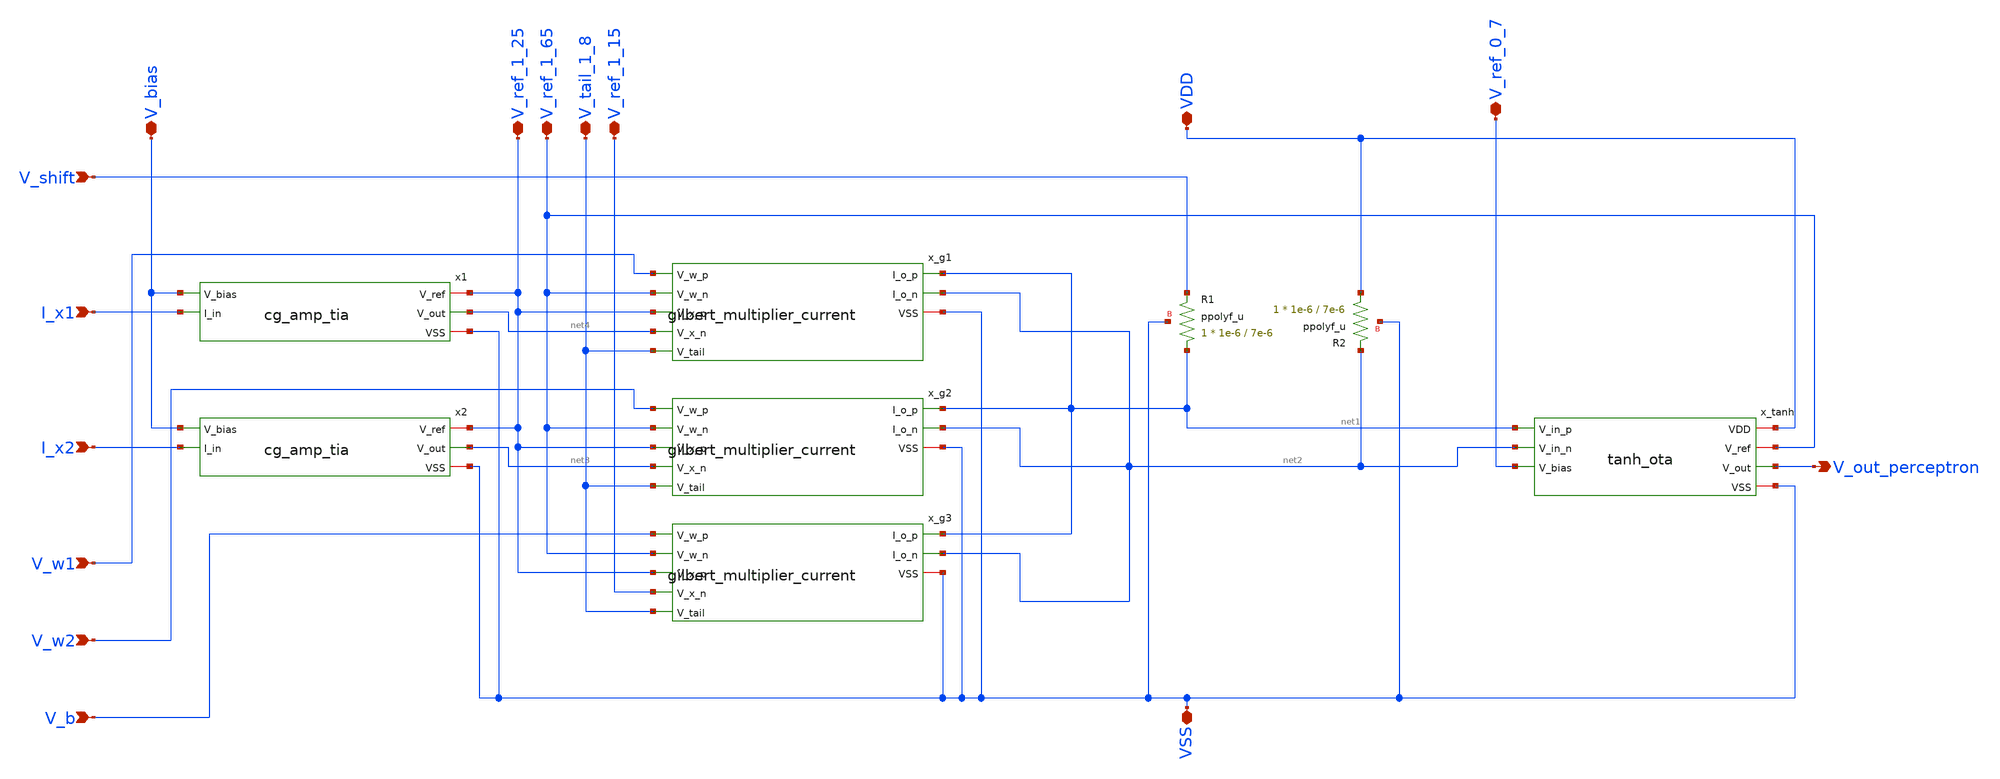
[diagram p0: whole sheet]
** sch_path: schematics/perceptron.sch
**.subckt perceptron VDD VSS V_bias I_x1 I_x2 V_ref_1_25 V_ref_1_15 V_ref_1_65 V_tail_1_8 V_w1 V_w2
*+ V_b V_ref_0_7 V_out_perceptron V_shift
*.iopin VDD
*.iopin VSS
*.iopin V_bias
*.ipin I_x1
*.ipin I_x2
*.iopin V_ref_1_25
*.iopin V_ref_1_15
*.iopin V_ref_1_65
*.iopin V_tail_1_8
*.ipin V_w1
*.ipin V_w2
*.ipin V_b
*.iopin V_ref_0_7
*.opin V_out_perceptron
*.ipin V_shift
x1 V_ref_1_25 net4 V_bias I_x1 VSS cg_amp_tia
x2 V_ref_1_25 net3 V_bias I_x2 VSS cg_amp_tia
x_g1 net1 net2 V_w1 V_ref_1_65 V_ref_1_25 net4 V_tail_1_8 VSS gilbert_multiplier_current
x_g2 net1 net2 V_w2 V_ref_1_65 V_ref_1_25 net3 V_tail_1_8 VSS gilbert_multiplier_current
x_g3 net1 net2 V_b V_ref_1_65 V_ref_1_25 V_ref_1_15 V_tail_1_8 VSS gilbert_multiplier_current
x_tanh VDD V_ref_1_65 V_out_perceptron net1 net2 V_ref_0_7 VSS tanh_ota
XR1 net1 V_shift VSS ppolyf_u r_width=1e-6 r_length=7e-6 m=1
XR2 VDD net2 VSS ppolyf_u r_width=1e-6 r_length=7e-6 m=1
**.ends

* expanding   symbol:  analog-perceptron-gf180mcu/schematics/cg_amp_tia.sym # of pins=5
** sym_path: schematics/cg_amp_tia.sym
** sch_path: schematics/cg_amp_tia.sch
.subckt cg_amp_tia V_ref V_out V_bias I_in VSS
*.iopin V_ref
*.iopin VSS
*.ipin I_in
*.ipin V_bias
*.opin V_out
XM1 V_out V_bias I_in VSS nfet_03v3 L=0.5u W=5u nf=1 ad='int((nf+1)/2) * W/nf * 0.18u' as='int((nf+2)/2) * W/nf * 0.18u'
+ pd='2*int((nf+1)/2) * (W/nf + 0.18u)' ps='2*int((nf+2)/2) * (W/nf + 0.18u)' nrd='0.18u / W' nrs='0.18u / W'
+ sa=0 sb=0 sd=0 m=1
XR1 V_out V_ref VSS ppolyf_u_1k r_width=3e-6 r_length=8.1e-6 m=1
.ends


* expanding   symbol:  analog-perceptron-gf180mcu/schematics/gilbert_multiplier_current.sym # of
*+ pins=8
** sym_path: schematics/gilbert_multiplier_current.sym
** sch_path: schematics/gilbert_multiplier_current.sch
.subckt gilbert_multiplier_current I_o_p I_o_n V_w_p V_w_n V_x_p V_x_n V_tail VSS
*.ipin V_x_p
*.ipin V_x_n
*.ipin V_tail
*.iopin VSS
*.ipin V_w_p
*.ipin V_w_n
*.opin I_o_n
*.opin I_o_p
XM1 net1 V_x_p net3 VSS nfet_03v3 L=0.5u W=10u nf=1 ad='int((nf+1)/2) * W/nf * 0.18u' as='int((nf+2)/2) * W/nf * 0.18u'
+ pd='2*int((nf+1)/2) * (W/nf + 0.18u)' ps='2*int((nf+2)/2) * (W/nf + 0.18u)' nrd='0.18u / W' nrs='0.18u / W'
+ sa=0 sb=0 sd=0 m=1
XM2 net2 V_x_n net4 VSS nfet_03v3 L=0.5u W=10u nf=1 ad='int((nf+1)/2) * W/nf * 0.18u' as='int((nf+2)/2) * W/nf * 0.18u'
+ pd='2*int((nf+1)/2) * (W/nf + 0.18u)' ps='2*int((nf+2)/2) * (W/nf + 0.18u)' nrd='0.18u / W' nrs='0.18u / W'
+ sa=0 sb=0 sd=0 m=1
XM3 I_o_n V_w_p net1 VSS nfet_03v3 L=0.5u W=10u nf=1 ad='int((nf+1)/2) * W/nf * 0.18u' as='int((nf+2)/2) * W/nf * 0.18u'
+ pd='2*int((nf+1)/2) * (W/nf + 0.18u)' ps='2*int((nf+2)/2) * (W/nf + 0.18u)' nrd='0.18u / W' nrs='0.18u / W'
+ sa=0 sb=0 sd=0 m=1
XM4 I_o_p V_w_n net1 VSS nfet_03v3 L=0.5u W=10u nf=1 ad='int((nf+1)/2) * W/nf * 0.18u' as='int((nf+2)/2) * W/nf * 0.18u'
+ pd='2*int((nf+1)/2) * (W/nf + 0.18u)' ps='2*int((nf+2)/2) * (W/nf + 0.18u)' nrd='0.18u / W' nrs='0.18u / W'
+ sa=0 sb=0 sd=0 m=1
XM5 I_o_n V_w_n net2 VSS nfet_03v3 L=0.5u W=10u nf=1 ad='int((nf+1)/2) * W/nf * 0.18u' as='int((nf+2)/2) * W/nf * 0.18u'
+ pd='2*int((nf+1)/2) * (W/nf + 0.18u)' ps='2*int((nf+2)/2) * (W/nf + 0.18u)' nrd='0.18u / W' nrs='0.18u / W'
+ sa=0 sb=0 sd=0 m=1
XM6 I_o_p V_w_p net2 VSS nfet_03v3 L=0.5u W=10u nf=1 ad='int((nf+1)/2) * W/nf * 0.18u' as='int((nf+2)/2) * W/nf * 0.18u'
+ pd='2*int((nf+1)/2) * (W/nf + 0.18u)' ps='2*int((nf+2)/2) * (W/nf + 0.18u)' nrd='0.18u / W' nrs='0.18u / W'
+ sa=0 sb=0 sd=0 m=1
XM7 net3 V_tail VSS VSS nfet_03v3 L=1u W=5u nf=1 ad='int((nf+1)/2) * W/nf * 0.18u' as='int((nf+2)/2) * W/nf * 0.18u'
+ pd='2*int((nf+1)/2) * (W/nf + 0.18u)' ps='2*int((nf+2)/2) * (W/nf + 0.18u)' nrd='0.18u / W' nrs='0.18u / W'
+ sa=0 sb=0 sd=0 m=1
XM8 net4 V_tail VSS VSS nfet_03v3 L=1u W=5u nf=1 ad='int((nf+1)/2) * W/nf * 0.18u' as='int((nf+2)/2) * W/nf * 0.18u'
+ pd='2*int((nf+1)/2) * (W/nf + 0.18u)' ps='2*int((nf+2)/2) * (W/nf + 0.18u)' nrd='0.18u / W' nrs='0.18u / W'
+ sa=0 sb=0 sd=0 m=1
XR1 net3 net4 VSS ppolyf_u_1k r_width=3e-6 r_length=46.2e-6 m=1
.ends


* expanding   symbol:  analog-perceptron-gf180mcu/schematics/tanh_ota.sym # of pins=7
** sym_path: schematics/tanh_ota.sym
** sch_path: schematics/tanh_ota.sch
.subckt tanh_ota VDD V_ref V_out V_in_p V_in_n V_bias VSS
*.iopin VDD
*.iopin VSS
*.ipin V_in_p
*.ipin V_in_n
*.ipin V_bias
*.opin V_out
*.iopin V_ref
XM1 net2 V_in_p net1 VSS nfet_03v3 L=0.5u W=10u nf=1 ad='int((nf+1)/2) * W/nf * 0.18u' as='int((nf+2)/2) * W/nf * 0.18u'
+ pd='2*int((nf+1)/2) * (W/nf + 0.18u)' ps='2*int((nf+2)/2) * (W/nf + 0.18u)' nrd='0.18u / W' nrs='0.18u / W'
+ sa=0 sb=0 sd=0 m=1
XM2 V_out V_in_n net1 VSS nfet_03v3 L=0.5u W=10u nf=1 ad='int((nf+1)/2) * W/nf * 0.18u' as='int((nf+2)/2) * W/nf * 0.18u'
+ pd='2*int((nf+1)/2) * (W/nf + 0.18u)' ps='2*int((nf+2)/2) * (W/nf + 0.18u)' nrd='0.18u / W' nrs='0.18u / W'
+ sa=0 sb=0 sd=0 m=1
XM3 net1 V_bias VSS VSS nfet_03v3 L=0.5u W=10u nf=1 ad='int((nf+1)/2) * W/nf * 0.18u' as='int((nf+2)/2) * W/nf * 0.18u'
+ pd='2*int((nf+1)/2) * (W/nf + 0.18u)' ps='2*int((nf+2)/2) * (W/nf + 0.18u)' nrd='0.18u / W' nrs='0.18u / W'
+ sa=0 sb=0 sd=0 m=1
XM4 net2 net2 VDD VDD pfet_03v3 L=0.5u W=20u nf=1 ad='int((nf+1)/2) * W/nf * 0.18u' as='int((nf+2)/2) * W/nf * 0.18u'
+ pd='2*int((nf+1)/2) * (W/nf + 0.18u)' ps='2*int((nf+2)/2) * (W/nf + 0.18u)' nrd='0.18u / W' nrs='0.18u / W'
+ sa=0 sb=0 sd=0 m=1
XM5 V_out net2 VDD VDD pfet_03v3 L=0.5u W=20u nf=1 ad='int((nf+1)/2) * W/nf * 0.18u' as='int((nf+2)/2) * W/nf * 0.18u'
+ pd='2*int((nf+1)/2) * (W/nf + 0.18u)' ps='2*int((nf+2)/2) * (W/nf + 0.18u)' nrd='0.18u / W' nrs='0.18u / W'
+ sa=0 sb=0 sd=0 m=1
XR1 net3 V_ref VSS ppolyf_u_1k r_width=3e-6 r_length=12.4e-6 m=1
XR2 net4 net3 VSS ppolyf_u_1k r_width=3e-6 r_length=12.4e-6 m=1
XR3 net5 net4 VSS ppolyf_u_1k r_width=3e-6 r_length=12.4e-6 m=1
XR4 net6 net5 VSS ppolyf_u_1k r_width=3e-6 r_length=12.4e-6 m=1
XR5 net7 net6 VSS ppolyf_u_1k r_width=3e-6 r_length=12.4e-6 m=1
XR6 V_out net7 VSS ppolyf_u_1k r_width=3e-6 r_length=12.4e-6 m=1
.ends

.end
